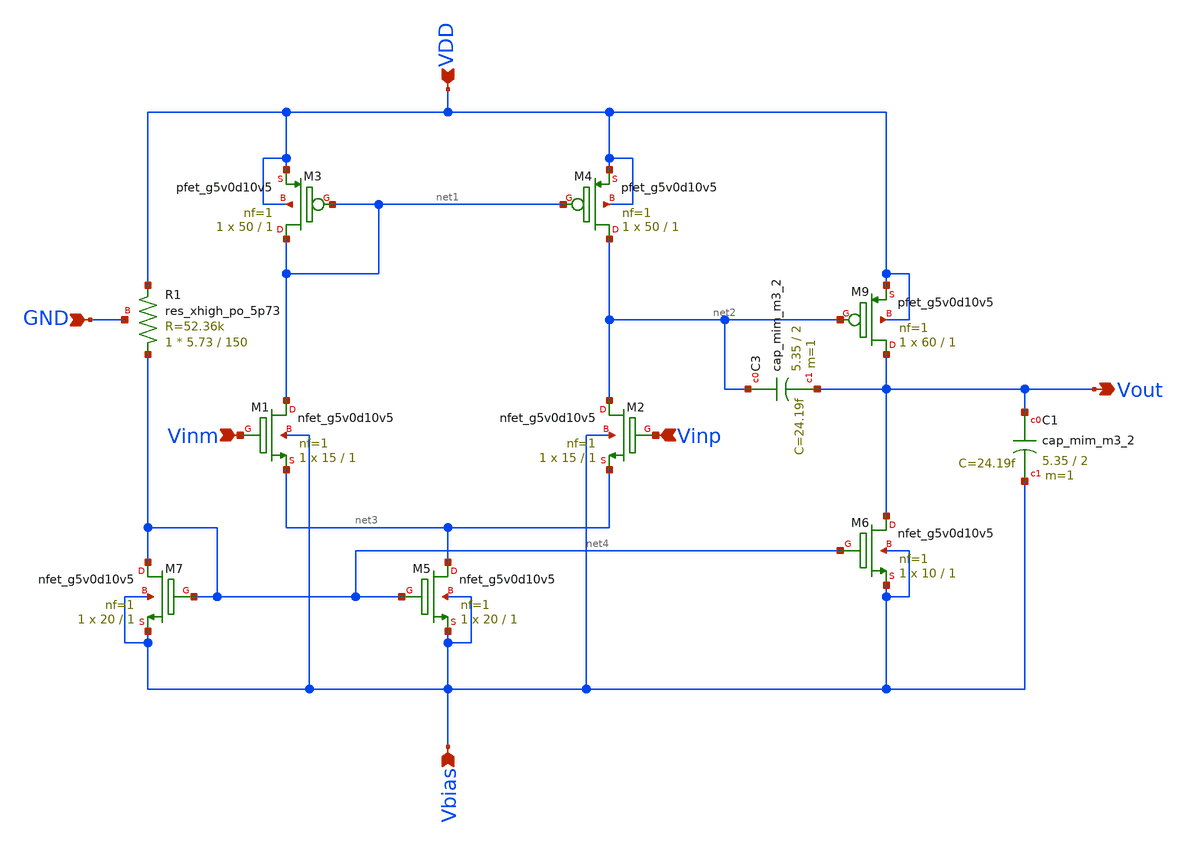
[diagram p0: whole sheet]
** sch_path: xschem/comparator.sch
**.subckt comparator Vout Vinp Vinm VDD Vbias GND
*.opin Vout
*.ipin Vinp
*.ipin Vinm
*.ipin VDD
*.ipin Vbias
*.ipin GND
XM9 Vout net2 VDD VDD sky130_fd_pr__pfet_g5v0d10v5 L=1 W=60 nf=1 ad='int((1 + 1)/2) * 60 / 1 * 0.29'
+ as='int((1 + 2)/2) * 60 / 1 * 0.29' pd='2*int((1 + 1)/2) * (60 / 1 + 0.29)' ps='2*int((1 + 2)/2) * (60 / 1 + 0.29)'
+ nrd='0.29 / 60 ' nrs='0.29 / 60 ' sa=0 sb=0 sd=0 mult=1 m=1
XM3 net1 net1 VDD VDD sky130_fd_pr__pfet_g5v0d10v5 L=1 W=50 nf=1 ad='int((1 + 1)/2) * 50 / 1 * 0.29'
+ as='int((1 + 2)/2) * 50 / 1 * 0.29' pd='2*int((1 + 1)/2) * (50 / 1 + 0.29)' ps='2*int((1 + 2)/2) * (50 / 1 + 0.29)'
+ nrd='0.29 / 50 ' nrs='0.29 / 50 ' sa=0 sb=0 sd=0 mult=1 m=1
XM4 net2 net1 VDD VDD sky130_fd_pr__pfet_g5v0d10v5 L=1 W=50 nf=1 ad='int((1 + 1)/2) * 50 / 1 * 0.29'
+ as='int((1 + 2)/2) * 50 / 1 * 0.29' pd='2*int((1 + 1)/2) * (50 / 1 + 0.29)' ps='2*int((1 + 2)/2) * (50 / 1 + 0.29)'
+ nrd='0.29 / 50 ' nrs='0.29 / 50 ' sa=0 sb=0 sd=0 mult=1 m=1
XM1 net1 Vinm net3 Vbias sky130_fd_pr__nfet_g5v0d10v5 L=1 W=15 nf=1 ad='int((1 + 1)/2) * 15 / 1 * 0.29'
+ as='int((1 + 2)/2) * 15 / 1 * 0.29' pd='2*int((1 + 1)/2) * (15 / 1 + 0.29)' ps='2*int((1 + 2)/2) * (15 / 1 + 0.29)'
+ nrd='0.29 / 15 ' nrs='0.29 / 15 ' sa=0 sb=0 sd=0 mult=1 m=1
XM2 net2 Vinp net3 Vbias sky130_fd_pr__nfet_g5v0d10v5 L=1 W=15 nf=1 ad='int((1 + 1)/2) * 15 / 1 * 0.29'
+ as='int((1 + 2)/2) * 15 / 1 * 0.29' pd='2*int((1 + 1)/2) * (15 / 1 + 0.29)' ps='2*int((1 + 2)/2) * (15 / 1 + 0.29)'
+ nrd='0.29 / 15 ' nrs='0.29 / 15 ' sa=0 sb=0 sd=0 mult=1 m=1
XM6 Vout net4 Vbias Vbias sky130_fd_pr__nfet_g5v0d10v5 L=1 W=10 nf=1 ad='int((1 + 1)/2) * 10 / 1 * 0.29'
+ as='int((1 + 2)/2) * 10 / 1 * 0.29' pd='2*int((1 + 1)/2) * (10 / 1 + 0.29)' ps='2*int((1 + 2)/2) * (10 / 1 + 0.29)'
+ nrd='0.29 / 10 ' nrs='0.29 / 10 ' sa=0 sb=0 sd=0 mult=1 m=1
XM5 net3 net4 Vbias Vbias sky130_fd_pr__nfet_g5v0d10v5 L=1 W=20 nf=1 ad='int((1 + 1)/2) * 20 / 1 * 0.29'
+ as='int((1 + 2)/2) * 20 / 1 * 0.29' pd='2*int((1 + 1)/2) * (20 / 1 + 0.29)' ps='2*int((1 + 2)/2) * (20 / 1 + 0.29)'
+ nrd='0.29 / 20 ' nrs='0.29 / 20 ' sa=0 sb=0 sd=0 mult=1 m=1
XM7 net4 net4 Vbias Vbias sky130_fd_pr__nfet_g5v0d10v5 L=1 W=20 nf=1 ad='int((1 + 1)/2) * 20 / 1 * 0.29'
+ as='int((1 + 2)/2) * 20 / 1 * 0.29' pd='2*int((1 + 1)/2) * (20 / 1 + 0.29)' ps='2*int((1 + 2)/2) * (20 / 1 + 0.29)'
+ nrd='0.29 / 20 ' nrs='0.29 / 20 ' sa=0 sb=0 sd=0 mult=1 m=1
XR1 net4 VDD GND sky130_fd_pr__res_xhigh_po_5p73 L=150 mult=1 m=1
XC3 net2 Vout sky130_fd_pr__cap_mim_m3_2 W=5.35 L=2 MF=1 m=1
XC1 Vout Vbias sky130_fd_pr__cap_mim_m3_2 W=5.35 L=2 MF=1 m=1
**.ends
.end
